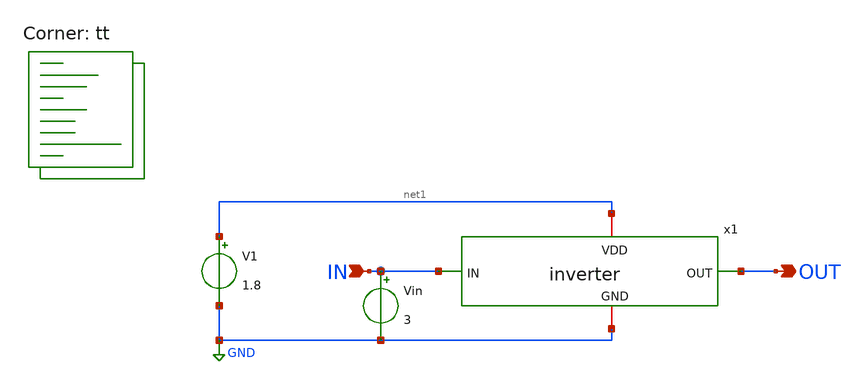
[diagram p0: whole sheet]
** sch_path: xschem/tb_dc.sch
**.subckt tb_dc OUT IN
*.opin OUT
*.ipin IN
x1 net1 IN OUT GND inverter
V1 net1 GND 1.8
Vin IN GND 3
**** begin user architecture code
.lib $::SKYWATER_MODELS/sky130.lib.spice tt


.save all
.control
  dc Vin 0 1.8 0.005
  write tb_dc.raw
.endc

**** end user architecture code
**.ends

* expanding   symbol:  inverter.sym # of pins=4
** sym_path: xschem/inverter.sym
** sch_path: xschem/inverter.sch
.subckt inverter VDD IN OUT GND
*.ipin IN
*.opin OUT
*.iopin VDD
*.iopin GND
XM1 OUT IN GND GND sky130_fd_pr__nfet_01v8 L=0.15 W=1 nf=1 ad='int((1 + 1)/2) * 1 / 1 * 0.29' as='int((1 + 2)/2) * 1 / 1 * 0.29'
+ pd='2*int((1 + 1)/2) * (1 / 1 + 0.29)' ps='2*int((1 + 2)/2) * (1 / 1 + 0.29)' nrd='0.29 / 1 ' nrs='0.29 / 1 '
+ sa=0 sb=0 sd=0 mult=1 m=1
XM2 OUT IN VDD VDD sky130_fd_pr__pfet_01v8 L=0.15 W=2 nf=1 ad='int((1 + 1)/2) * 2 / 1 * 0.29' as='int((1 + 2)/2) * 2 / 1 * 0.29'
+ pd='2*int((1 + 1)/2) * (2 / 1 + 0.29)' ps='2*int((1 + 2)/2) * (2 / 1 + 0.29)' nrd='0.29 / 2 ' nrs='0.29 / 2 '
+ sa=0 sb=0 sd=0 mult=1 m=1
.ends

.GLOBAL GND
.end
